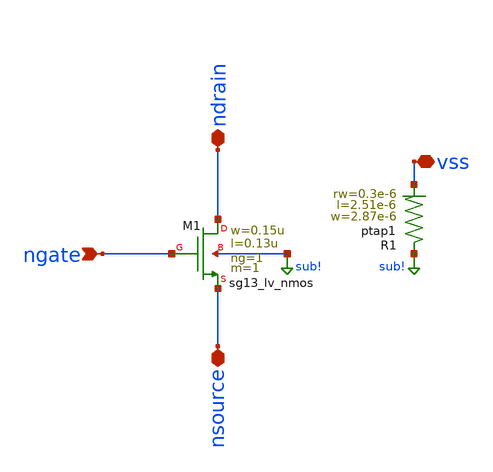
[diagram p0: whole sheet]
** sch_path: ihp-sg13g2/libs.tech/klayout/sg13g2_tests/lvs_testcases/nmos_sub_test.sch
**.subckt nmos_sub_test vss ngate ndrain nsource
*.iopin vss
*.ipin ngate
*.iopin ndrain
*.iopin nsource
XM1 ndrain ngate nsource sub! sg13_lv_nmos w=0.15u l=0.13u ng=1 m=1 mm_ok=1
XR1 sub! vss ptap1 R=23.84 w=2.87e-6 l=2.51e-6
**.ends
.GLOBAL sub!
.end
